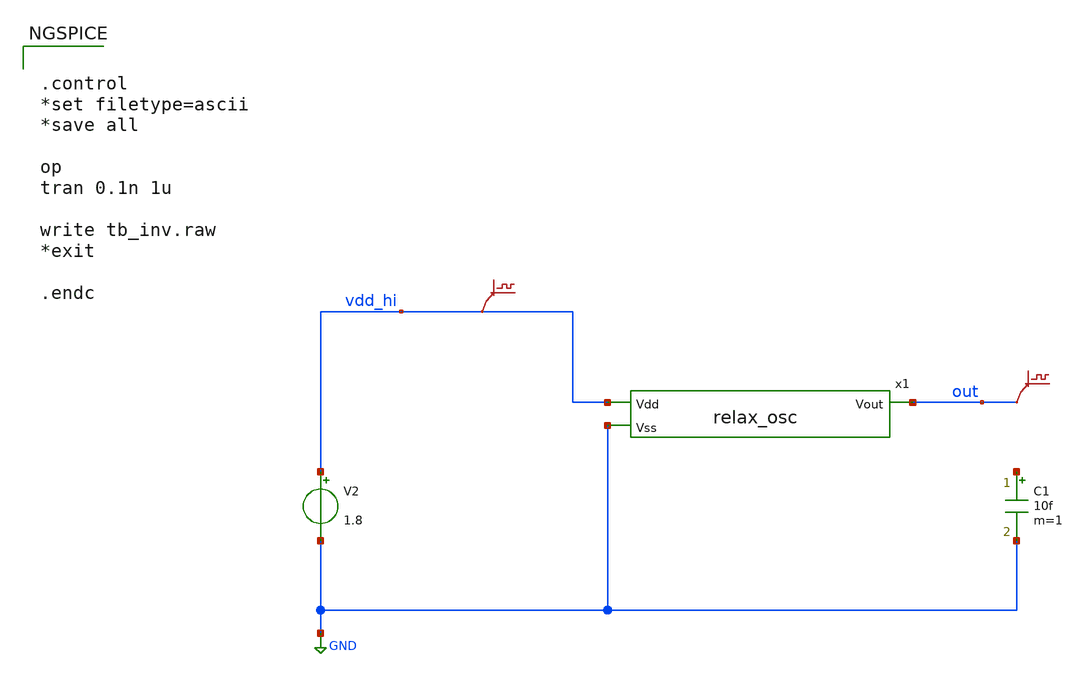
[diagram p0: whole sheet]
** sch_path: xschem/relax_osc_tb.sch
**.subckt relax_osc_tb
V2 vdd_hi GND 1.8
C1 net1 GND 10f m=1
.save v(vdd_hi)
.save v(out)
x1 vdd_hi GND out relax_osc
**** begin user architecture code


.control
*set filetype=ascii
*save all

op
tran 0.1n 1u

write tb_inv.raw
*exit

.endc



** opencircuitdesign pdks install
.lib $::SKYWATER_MODELS/sky130.lib.spice tt


**** end user architecture code
**.ends
.GLOBAL GND
.end
